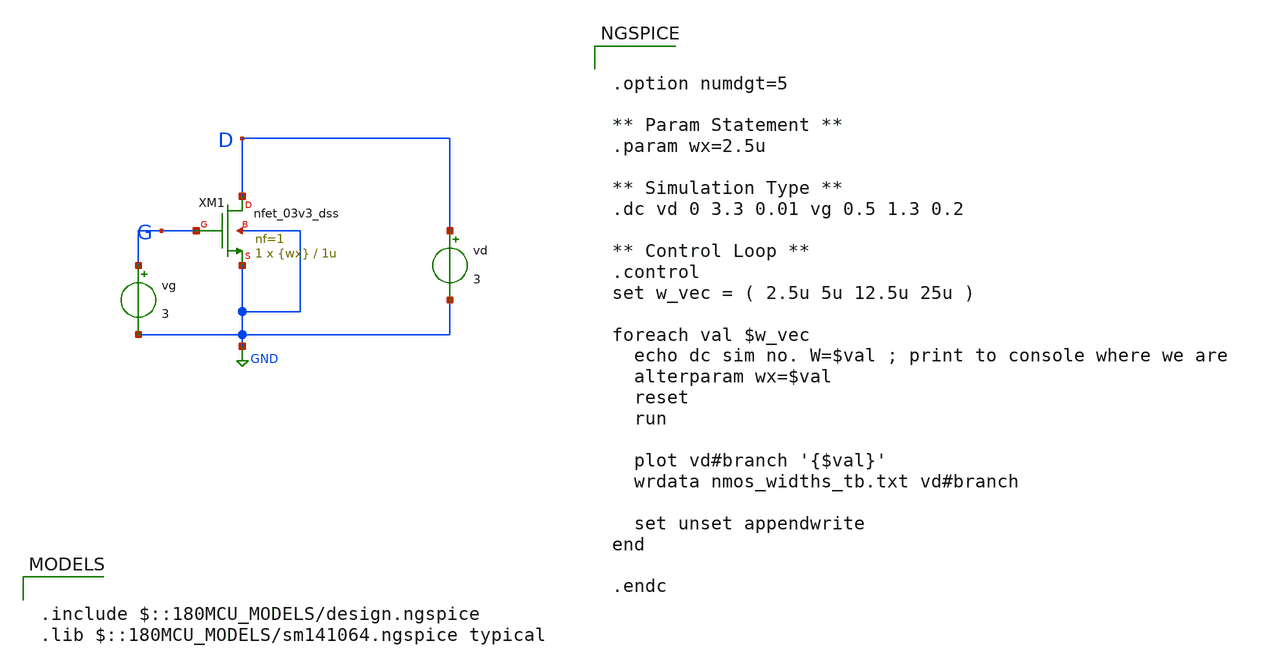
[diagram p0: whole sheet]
** sch_path: designs/switch_matrix_gf180mcu_9t5v0-main/designs/libs/tb_analog/unit_transistors/nmos_widths_tb.sch
**.subckt nmos_widths_tb
XM1 D G GND GND nfet_03v3_dss L=1u W={wx} nf=1 ad='int((nf+1)/2) * W/nf * 0.18u' as='int((nf+2)/2) * W/nf * 0.18u'
+ pd='2*int((nf+1)/2) * (W/nf + 0.18u)' ps='2*int((nf+2)/2) * (W/nf + 0.18u)' nrd='0.18u / W' nrs='0.18u / W'
+ sa=0 sb=0 sd=0 m=1
vd D GND 3
vg G GND 3
**** begin user architecture code

.include $::180MCU_MODELS/design.ngspice
.lib $::180MCU_MODELS/sm141064.ngspice typical



.option numdgt=5

** Param Statement **
.param wx=2.5u

** Simulation Type **
.dc vd 0 3.3 0.01 vg 0.5 1.3 0.2

** Control Loop **
.control
set w_vec = ( 2.5u 5u 12.5u 25u )

foreach val $w_vec
  echo dc sim no. W=$val ; print to console where we are
  alterparam wx=$val
  reset
  run

  plot vd#branch '{$val}'
  wrdata nmos_widths_tb.txt vd#branch

  set unset appendwrite
end

.endc


**** end user architecture code
**.ends
.GLOBAL GND
.end
